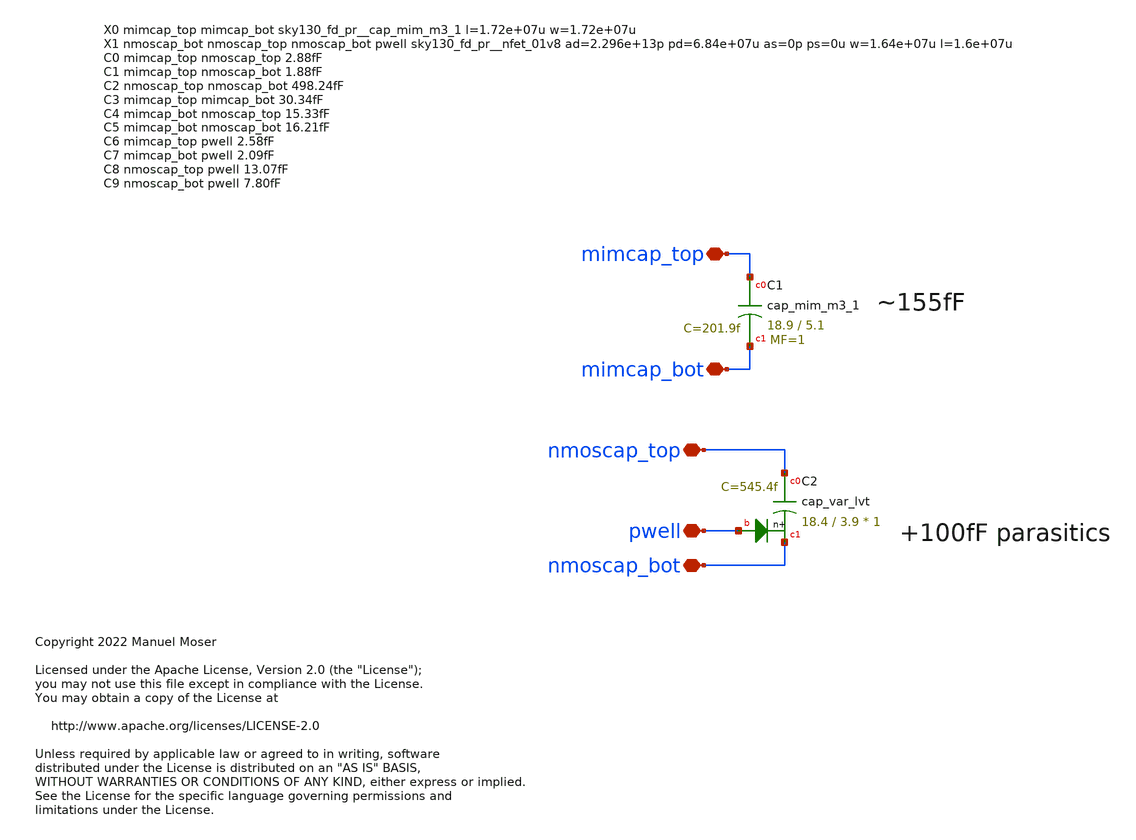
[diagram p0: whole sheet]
** sch_path: xschem/adc_noise_decoup_cell2.sch
* Copyright 2022 Manuel Moser
* Licensed under the Apache License, Version 2.0 (the "License");
**.subckt adc_noise_decoup_cell2 nmoscap_top mimcap_top mimcap_bot nmoscap_bot pwell
*.iopin nmoscap_top
*.iopin mimcap_top
*.iopin mimcap_bot
*.iopin nmoscap_bot
*.iopin pwell
XC1 mimcap_top mimcap_bot sky130_fd_pr__cap_mim_m3_1 W=18.9 L=5.1 MF=1 m=1
XC2 nmoscap_top nmoscap_bot pwell sky130_fd_pr__cap_var_lvt W=18.4 L=3.9 VM=1 m=1
**.ends
.end
